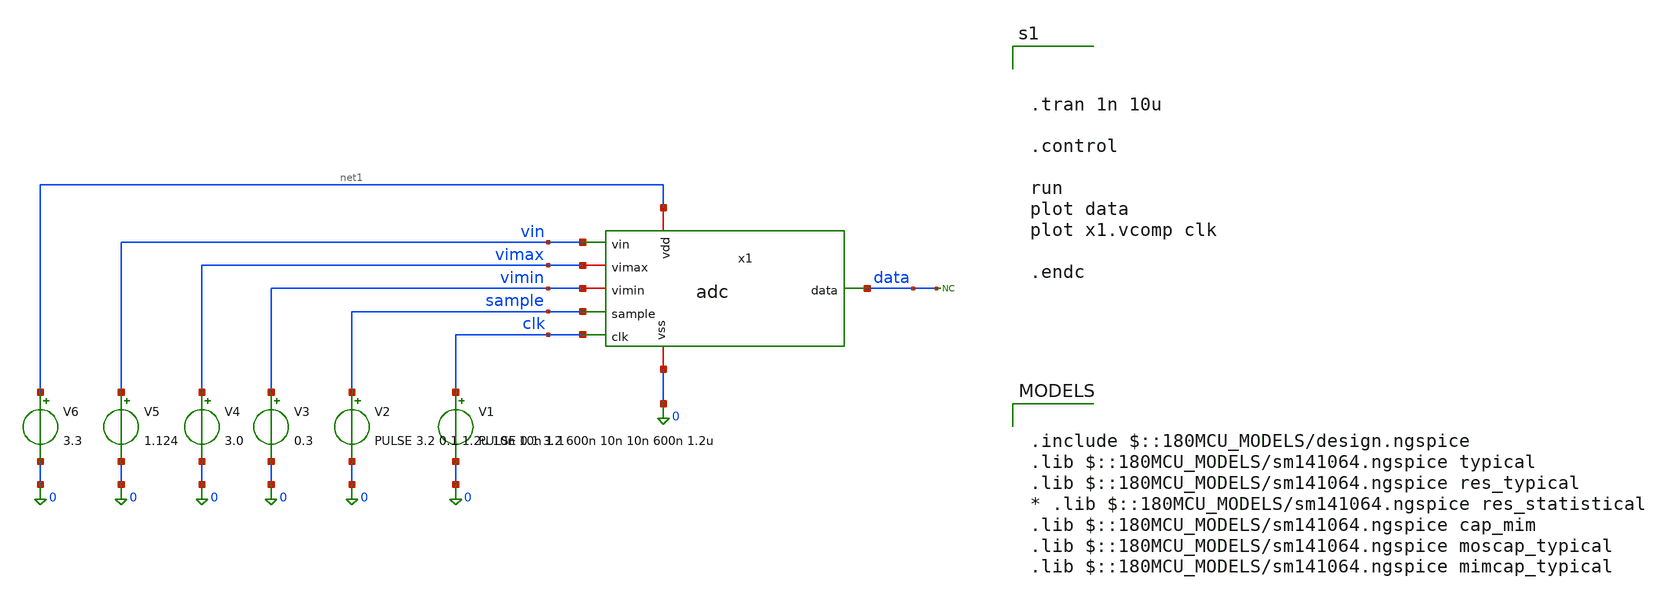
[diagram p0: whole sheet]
** sch_path: General/ADC/adc_tb.sch
**.subckt adc_tb
x1 vin sample data clk net1 vimax vimin 0 adc
V1 clk 0 PULSE 0.1 3.2 600n 10n 10n 600n 1.2u
V2 sample 0 PULSE 3.2 0.1 1.2u 10n 10n 1 1
V3 vimin 0 0.3
V4 vimax 0 3.0
V5 vin 0 1.124
V6 net1 0 3.3
* noconn data
**** begin user architecture code

.include $::180MCU_MODELS/design.ngspice
.lib $::180MCU_MODELS/sm141064.ngspice typical
.lib $::180MCU_MODELS/sm141064.ngspice res_typical
* .lib $::180MCU_MODELS/sm141064.ngspice res_statistical
.lib $::180MCU_MODELS/sm141064.ngspice cap_mim
.lib $::180MCU_MODELS/sm141064.ngspice moscap_typical
.lib $::180MCU_MODELS/sm141064.ngspice mimcap_typical




.tran 1n 10u

.control

run
plot data
plot x1.vcomp clk

.endc



**** end user architecture code
**.ends
.end
